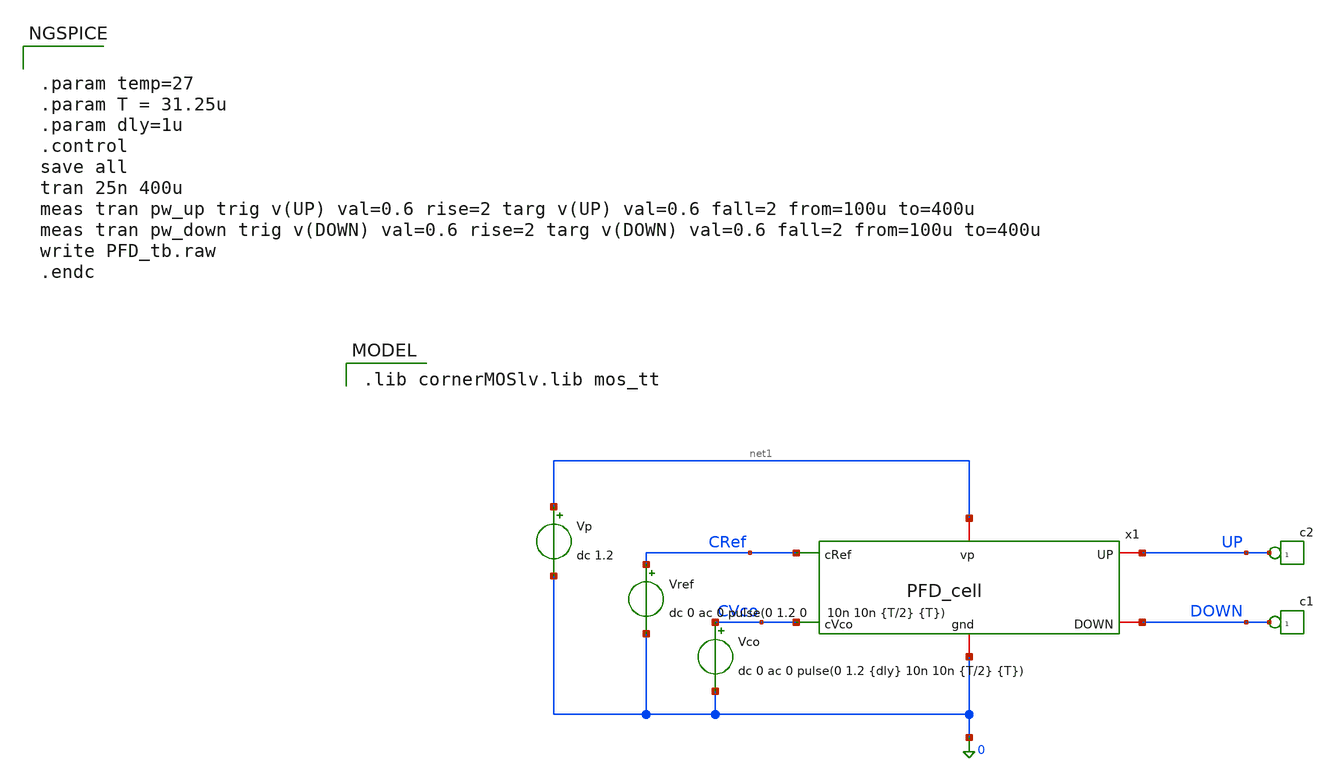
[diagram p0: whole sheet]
** sch_path: PFD/PFD_tb.sch
**.subckt PFD_tb
x1 0 net1 CRef UP DOWN CVco PFD_cell
*connector(1,1) ?1 DOWN
*connector(1,1) ?1 UP
Vref CRef 0 dc 0 ac 0 pulse(0 1.2 0 10n 10n {T/2} {T})
Vco CVco 0 dc 0 ac 0 pulse(0 1.2 {dly} 10n 10n {T/2} {T})
Vp net1 0 dc 1.2
**** begin user architecture code
 .lib cornerMOSlv.lib mos_tt



.param temp=27
.param T = 31.25u
.param dly=1u
.control
save all
tran 25n 400u
meas tran pw_up trig v(UP) val=0.6 rise=2 targ v(UP) val=0.6 fall=2 from=100u to=400u
meas tran pw_down trig v(DOWN) val=0.6 rise=2 targ v(DOWN) val=0.6 fall=2 from=100u to=400u
write PFD_tb.raw
.endc


**** end user architecture code
**.ends
.end
